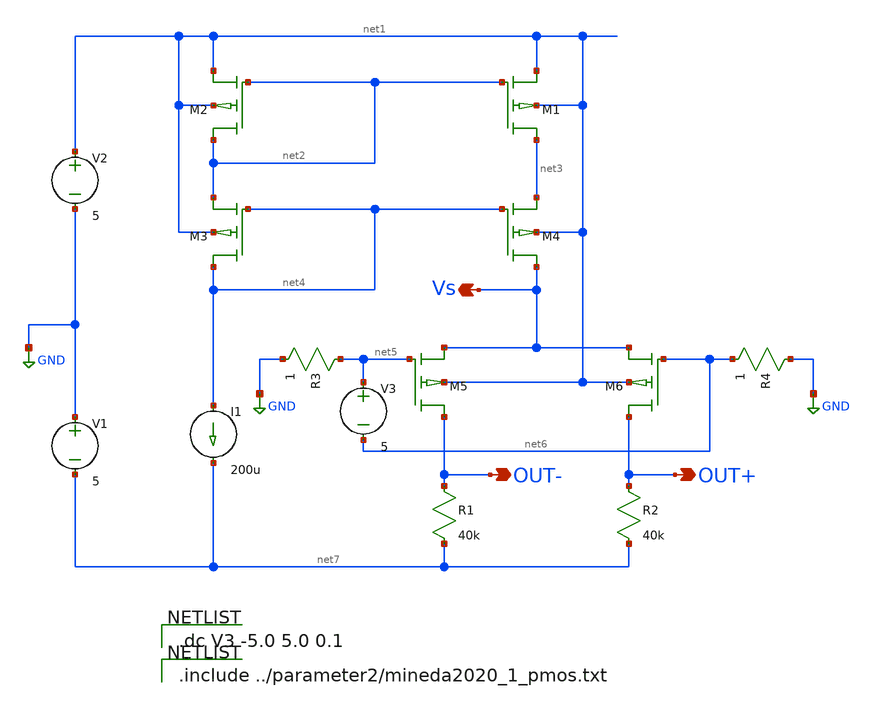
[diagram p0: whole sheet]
** sch_path: diffamp_test10umrealCS.sch
**.subckt diffamp_test10umrealCS Vs OUT+ OUT-
*.opin Vs
*.opin OUT+
*.opin OUT-
V1 GND net7 5
M1 net3 net2 net1 net1 YSS_PMOS w=14u l=14u as=0 ps=0 ad=0 pd=0 m=20
V2 net1 GND 5
I1 net4 net7 200u
M2 net2 net2 net1 net1 YSS_PMOS w=14u l=14u as=0 ps=0 ad=0 pd=0 m=20
V3 net5 net6 5
M3 net4 net4 net2 net1 YSS_PMOS w=14u l=14u as=0 ps=0 ad=0 pd=0 m=20
M4 Vs net4 net3 net1 YSS_PMOS w=14u l=14u as=0 ps=0 ad=0 pd=0 m=20
M5 OUT- net5 Vs net1 YSS_PMOS w=10u l=10u as=0 ps=0 ad=0 pd=0 m=10
M6 OUT+ net6 Vs net1 YSS_PMOS w=10u l=10u as=0 ps=0 ad=0 pd=0 m=10
R1 OUT- net7 40k m=1
R2 OUT+ net7 40k m=1
R3 net5 GND 1 m=1
R4 GND net6 1 m=1
**** begin user architecture code

.dc V3 -5.0 5.0 0.1


.include ../parameter2/mineda2020_1_pmos.txt

**** end user architecture code
**.ends
.GLOBAL GND
.end
